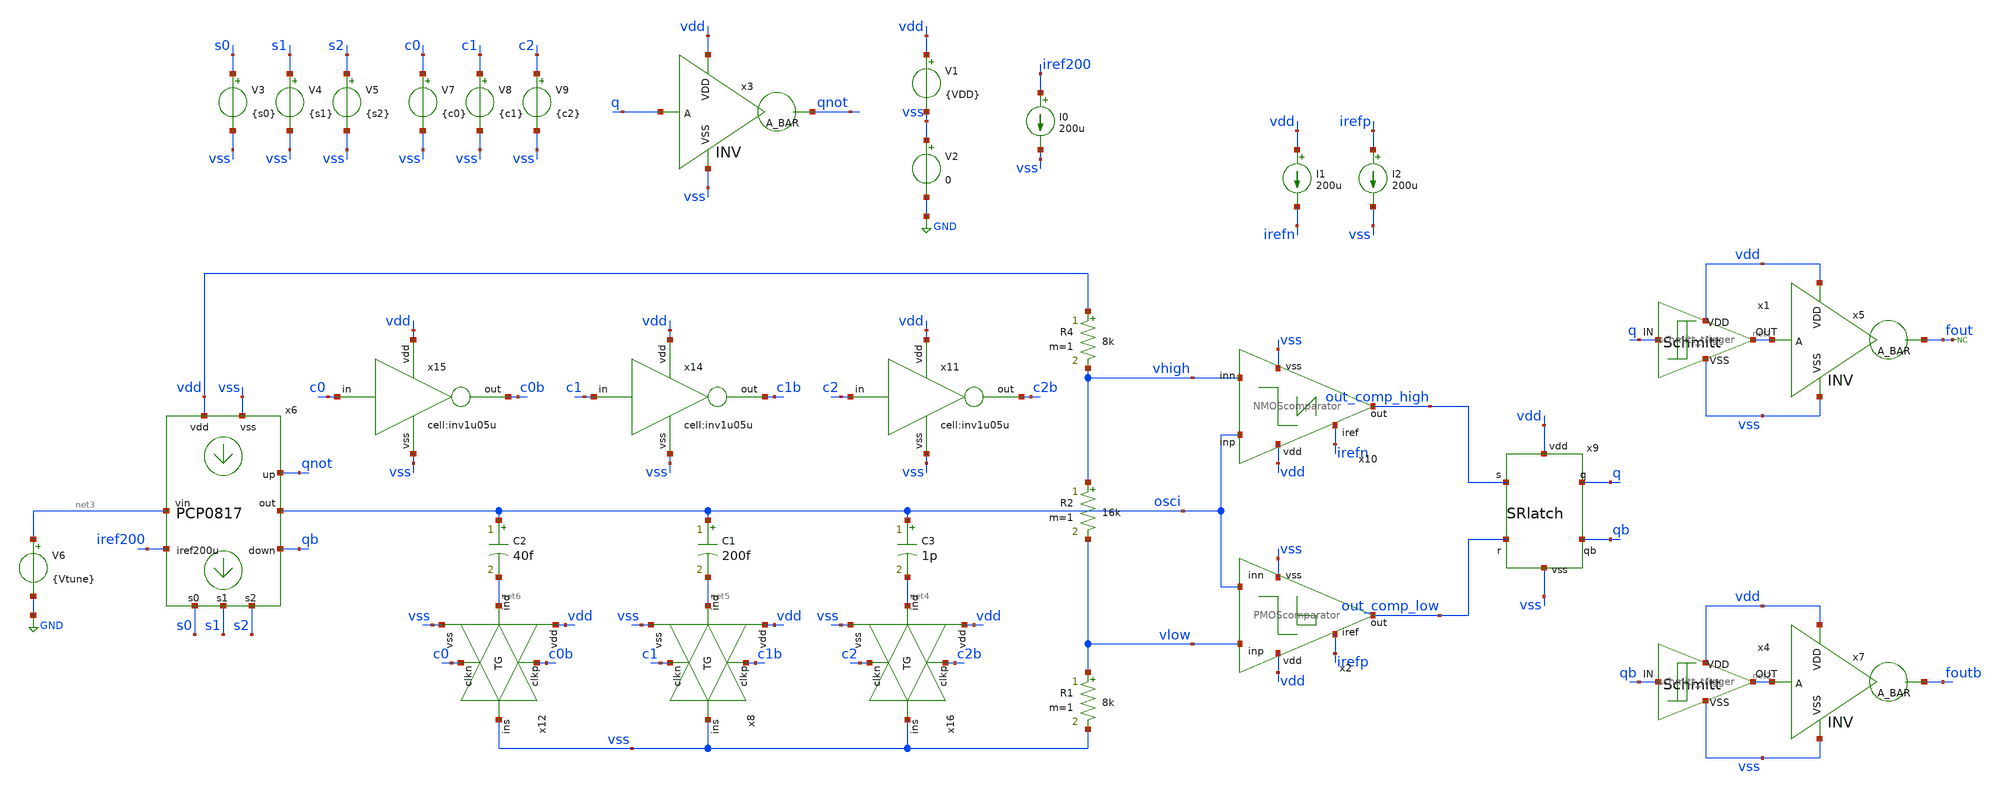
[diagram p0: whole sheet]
** sch_path: designs/libs/qw_core_analog/VCO0818/VCO0818.sch
**.subckt VCO0818
V1 vdd vss {VDD}
V2 vss GND 0
I1 vdd irefn 200u
I2 irefp vss 200u
R1 vlow vss 8k m=1
R2 vhigh vlow 16k m=1
R4 vdd vhigh 8k m=1
x9 vdd out_comp_high q qb out_comp_low vss SRlatch
x2 vdd irefp vlow out_comp_low osci vss PMOScomparator
x10 vdd osci out_comp_high vhigh irefn vss NMOScomparator
x3 vdd q qnot vss INV
x1 q net1 vdd vss schmitt_trigger
x4 qb net2 vdd vss schmitt_trigger
x5 vdd net1 fout vss INV
x7 vdd net2 foutb vss INV
V6 net3 GND {Vtune}
I0 iref200 vss 200u
* noconn fout
V3 s0 vss {s0}
V4 s1 vss {s1}
V5 s2 vss {s2}
V7 c0 vss {c0}
V8 c1 vss {c1}
V9 c2 vss {c2}
C3 osci net4 1p m=1
x11 c2 vdd c2b vss inv1u05u
x6 vdd vss net3 iref200 osci qnot qb s0 s1 s2 PCP0817
C1 osci net5 200f m=1
C2 osci net6 40f m=1
x14 c1 vdd c1b vss inv1u05u
x15 c0 vdd c0b vss inv1u05u
x16 vdd c2b net4 vss vss c2 TG
x8 vdd c1b net5 vss vss c1 TG
x12 vdd c0b net6 vss vss c0 TG
**** begin user architecture code



.param VDD = 3.3
.param Vtune = 2.7
.param s0 = 3.3 s1 = 0 s2 = 0 c0 = 0 c1 = 0 c2 = 3.3
.param VIN=1
*V6 net3 0 {Vtune}
.meas tran period1 TRIG v(fout) VAL=1.65 RISE=15 TARG v(fout) VAL=1.65 RISE=16
.meas tran freq param='1/period1'

.control
save all

let vstart = 0.0
let vstop = 3.3
let vstep = 0.1

foreach VINVAL 2.1 2.2
    alterparam Vtune = $VINVAL
    reset
    tran 10p 200n
end

write VCO0818.raw
.endc



.include $::180MCU_MODELS/design.ngspice
.lib $::180MCU_MODELS/sm141064.ngspice typical
.lib $::180MCU_MODELS/sm141064.ngspice cap_mim
.lib $::180MCU_MODELS/sm141064.ngspice res_typical
.lib $::180MCU_MODELS/sm141064.ngspice moscap_typical
.lib $::180MCU_MODELS/sm141064.ngspice mimcap_typical
* .lib $::180MCU_MODELS/sm141064.ngspice res_statistical

**** end user architecture code
**.ends
.GLOBAL GND
.end
